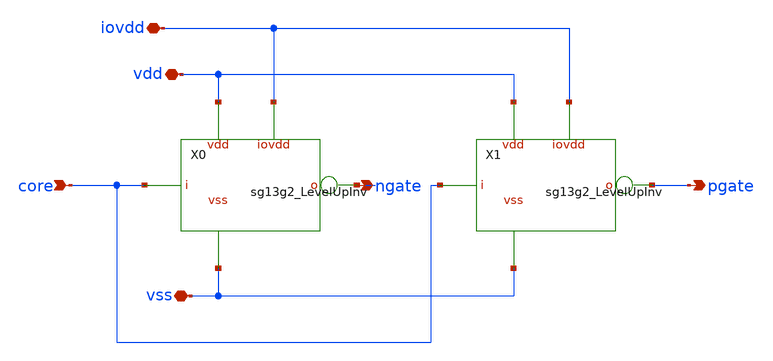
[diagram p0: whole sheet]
** sch_path: ihp-sg13g2/libs.ref/sg13g2_io/sch/xschem/sg13g2_GateLevelUpInv.sch
**.subckt sg13g2_GateLevelUpInv pgate core ngate vss vdd iovdd
*.opin pgate
*.ipin core
*.opin ngate
*.iopin vss
*.iopin vdd
*.iopin iovdd
X0 core ngate vss vdd iovdd sg13g2_LevelUpInv
X1 core pgate vss vdd iovdd sg13g2_LevelUpInv
**.ends
.end
